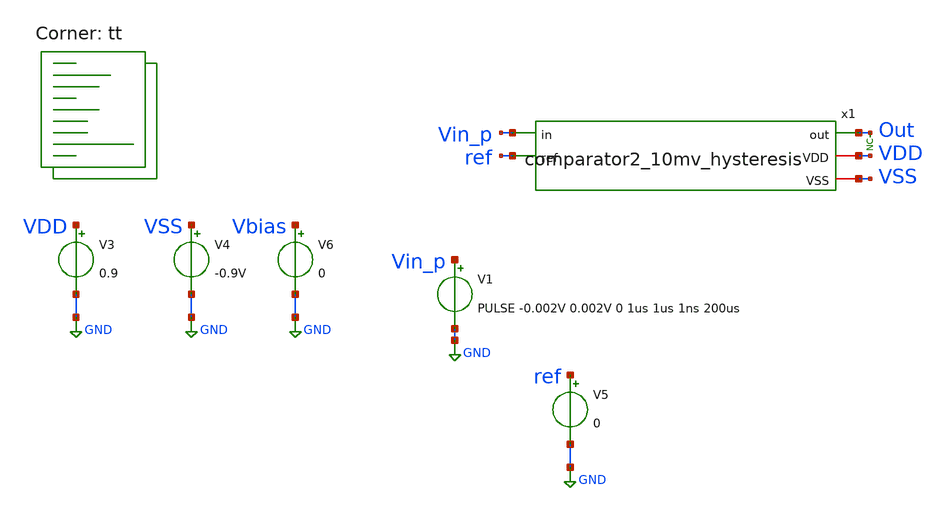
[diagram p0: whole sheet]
** sch_path: xschem/tests/comparator2/comparator2_with_hysteresis_test.sch
**.subckt comparator2_with_hysteresis_test
V3 VDD GND 0.9
V4 VSS GND -0.9V
V1 Vin_p GND PULSE -0.002V 0.002V 0 1us 1us 1ns 200us
V6 Vbias GND 0
V5 ref GND 0
* noconn Out
x1 Out VDD VSS Vin_p ref comparator2_10mv_hysteresis
**** begin user architecture code
 *.lib $::SKYWATER_MODELS/sky130.lib.spice tt
.include $::SKYWATER_STDCELLS/sky130_fd_sc_hd.spice



* Here's a comment
.options acct list
.options method=gear
.temp 25
*vvcc VDD 0 dc 1.8
*vvss VSS 0 0
.control
save all
tran 0.001u 2u
plot Vin_p 0.002*out ref
plot x1.net2
write comparator2_with_hysteresis_test.raw
.endc


.lib $::SKYWATER_MODELS/sky130.lib.spice tt
**** end user architecture code
**.ends

* expanding   symbol:  src/comparator2/comparator2_10mv_hysteresis.sym # of pins=5
** sym_path: xschem/src/comparator2/comparator2_10mv_hysteresis.sym
** sch_path: xschem/src/comparator2/comparator2_10mv_hysteresis.sch
.subckt comparator2_10mv_hysteresis out VDD VSS in ref
*.iopin VDD
*.ipin in
*.opin out
*.iopin VSS
*.ipin ref
XM4 net1 net1 VDD VDD sky130_fd_pr__pfet_01v8 L=0.25 W=10 nf=4 ad='int((nf+1)/2) * W/nf * 0.29' as='int((nf+2)/2)
+ * W/nf * 0.29' pd='2*int((nf+1)/2) * (W/nf + 0.29)' ps='2*int((nf+2)/2) * (W/nf + 0.29)' nrd='0.29 /
+ W' nrs='0.29 / W' sa=0 sb=0 sd=0 mult=1 m=1
XM5 net2 net1 VDD VDD sky130_fd_pr__pfet_01v8 L=0.25 W=10 nf=4 ad='int((nf+1)/2) * W/nf * 0.29' as='int((nf+2)/2)
+ * W/nf * 0.29' pd='2*int((nf+1)/2) * (W/nf + 0.29)' ps='2*int((nf+2)/2) * (W/nf + 0.29)' nrd='0.29 /
+ W' nrs='0.29 / W' sa=0 sb=0 sd=0 mult=1 m=1
XM6 net1 net2 VDD VDD sky130_fd_pr__pfet_01v8 L=0.25 W=10 nf=4 ad='int((nf+1)/2) * W/nf * 0.29' as='int((nf+2)/2)
+ * W/nf * 0.29' pd='2*int((nf+1)/2) * (W/nf + 0.29)' ps='2*int((nf+2)/2) * (W/nf + 0.29)' nrd='0.29 /
+ W' nrs='0.29 / W' sa=0 sb=0 sd=0 mult=1 m=1
XM10 net3 net4 VSS VSS sky130_fd_pr__nfet_01v8 L=0.5 W=20 nf=4 ad='int((nf+1)/2) * W/nf * 0.29' as='int((nf+2)/2)
+ * W/nf * 0.29' pd='2*int((nf+1)/2) * (W/nf + 0.29)' ps='2*int((nf+2)/2) * (W/nf + 0.29)' nrd='0.29 /
+ W' nrs='0.29 / W' sa=0 sb=0 sd=0 mult=1 m=1
XM11 VSS net4 net4 VSS sky130_fd_pr__nfet_01v8 L=2 W=20 nf=4 ad='int((nf+1)/2) * W/nf * 0.29' as='int((nf+2)/2)
+ * W/nf * 0.29' pd='2*int((nf+1)/2) * (W/nf + 0.29)' ps='2*int((nf+2)/2) * (W/nf + 0.29)' nrd='0.29 /
+ W' nrs='0.29 / W' sa=0 sb=0 sd=0 mult=1 m=1
XM12 net5 net4 VSS VSS sky130_fd_pr__nfet_01v8 L=2.0 W=4 nf=4 ad='int((nf+1)/2) * W/nf * 0.29' as='int((nf+2)/2)
+ * W/nf * 0.29' pd='2*int((nf+1)/2) * (W/nf + 0.29)' ps='2*int((nf+2)/2) * (W/nf + 0.29)' nrd='0.29 /
+ W' nrs='0.29 / W' sa=0 sb=0 sd=0 mult=1 m=1
XM13 out net5 VDD VDD sky130_fd_pr__pfet_01v8 L=0.5 W=2 nf=1 ad='int((nf+1)/2) * W/nf * 0.29' as='int((nf+2)/2)
+ * W/nf * 0.29' pd='2*int((nf+1)/2) * (W/nf + 0.29)' ps='2*int((nf+2)/2) * (W/nf + 0.29)' nrd='0.29 /
+ W' nrs='0.29 / W' sa=0 sb=0 sd=0 mult=1 m=1
XM14 out net5 VSS VSS sky130_fd_pr__nfet_01v8 L=0.5 W=2 nf=1 ad='int((nf+1)/2) * W/nf * 0.29' as='int((nf+2)/2)
+ * W/nf * 0.29' pd='2*int((nf+1)/2) * (W/nf + 0.29)' ps='2*int((nf+2)/2) * (W/nf + 0.29)' nrd='0.29 /
+ W' nrs='0.29 / W' sa=0 sb=0 sd=0 mult=1 m=1
XM15 net2 net2 VDD VDD sky130_fd_pr__pfet_01v8 L=0.25 W=10 nf=4 ad='int((nf+1)/2) * W/nf * 0.29' as='int((nf+2)/2)
+ * W/nf * 0.29' pd='2*int((nf+1)/2) * (W/nf + 0.29)' ps='2*int((nf+2)/2) * (W/nf + 0.29)' nrd='0.29 /
+ W' nrs='0.29 / W' sa=0 sb=0 sd=0 mult=1 m=1
I0 VDD net4 20u
XM2 net5 net2 VDD VDD sky130_fd_pr__pfet_01v8 L=1 W=2 nf=1 ad='int((nf+1)/2) * W/nf * 0.29' as='int((nf+2)/2)
+ * W/nf * 0.29' pd='2*int((nf+1)/2) * (W/nf + 0.29)' ps='2*int((nf+2)/2) * (W/nf + 0.29)' nrd='0.29 /
+ W' nrs='0.29 / W' sa=0 sb=0 sd=0 mult=1 m=1
XM1 net1 in net3 VSS sky130_fd_pr__nfet_01v8 L=0.15 W=15 nf=4 ad='int((nf+1)/2) * W/nf * 0.29' as='int((nf+2)/2)
+ * W/nf * 0.29' pd='2*int((nf+1)/2) * (W/nf + 0.29)' ps='2*int((nf+2)/2) * (W/nf + 0.29)' nrd='0.29 /
+ W' nrs='0.29 / W' sa=0 sb=0 sd=0 mult=1 m=1
XM3 net2 ref net3 VSS sky130_fd_pr__nfet_01v8 L=0.15 W=15 nf=4 ad='int((nf+1)/2) * W/nf * 0.29' as='int((nf+2)/2)
+ * W/nf * 0.29' pd='2*int((nf+1)/2) * (W/nf + 0.29)' ps='2*int((nf+2)/2) * (W/nf + 0.29)' nrd='0.29 /
+ W' nrs='0.29 / W' sa=0 sb=0 sd=0 mult=1 m=1
.ends

.GLOBAL GND
.end
